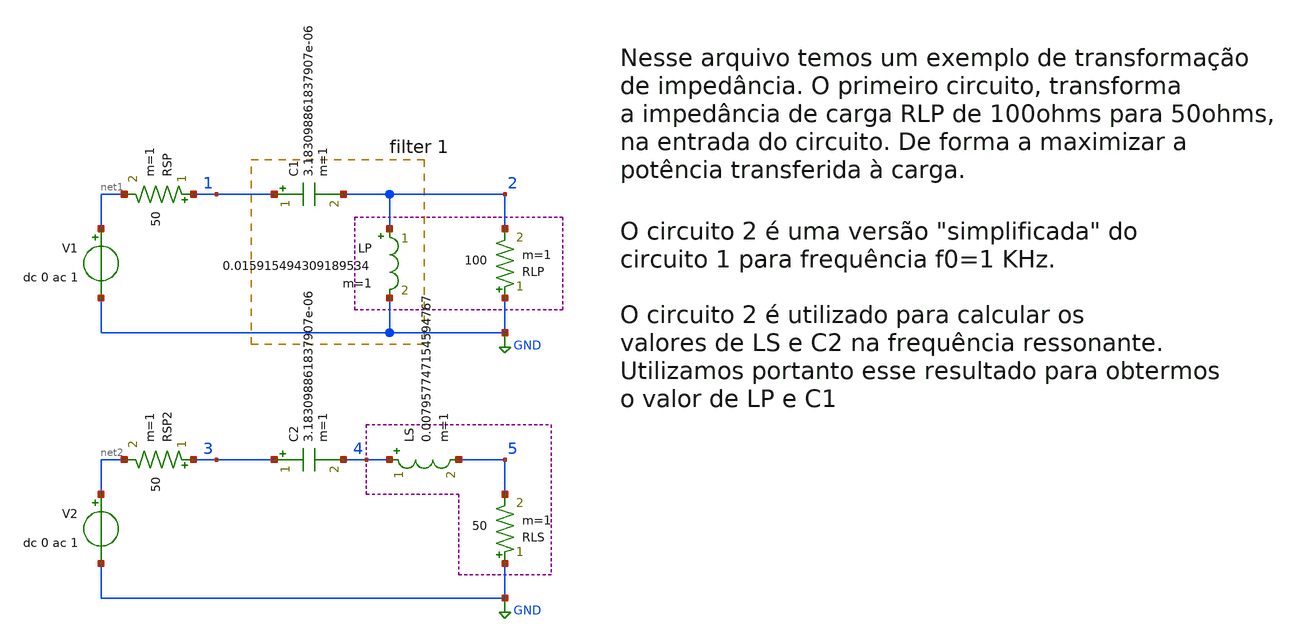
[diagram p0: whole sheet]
** sch_path: circuitos/exemplo04.sch
**.subckt exemplo04
C1 1 2 3.183098861837907e-06 m=1
V1 net1 GND dc 0 ac 1
RLP GND 2 100 m=1
RSP 1 net1 50 m=1
LP 2 GND 0.015915494309189534 m=1
C2 3 4 3.183098861837907e-06 m=1
V2 net2 GND dc 0 ac 1
RLS GND 5 50 m=1
RSP2 3 net2 50 m=1
LS 4 5 0.007957747154594767 m=1
**** begin user architecture code

.control
op
ac dec 1e3 1e2 1e4

setplot ac1
plot (v(3)/v2#branch)
plot real(v(1)/-v1#branch)
plot imag(v(1)/-v1#branch)
.endc

**** end user architecture code
**.ends
.GLOBAL GND
.end
